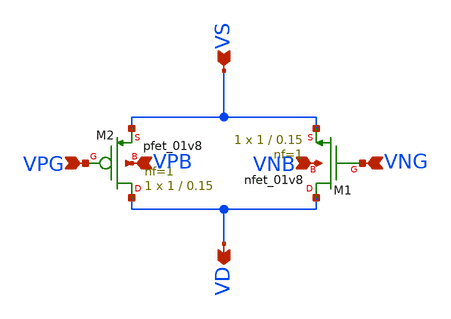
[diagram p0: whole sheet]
** sch_path: analog/schematics/Aswitch.sch
**.subckt Aswitch VPG VPB VNB VNG VS VD
*.ipin VPG
*.ipin VPB
*.ipin VNB
*.ipin VNG
*.ipin VS
*.opin VD
XM1 VD VNG VS VNB sky130_fd_pr__nfet_01v8 L=0.15 W=1 nf=1 ad='int((nf+1)/2) * W/nf * 0.29' as='int((nf+2)/2) * W/nf * 0.29'
+ pd='2*int((nf+1)/2) * (W/nf + 0.29)' ps='2*int((nf+2)/2) * (W/nf + 0.29)' nrd='0.29 / W' nrs='0.29 / W'
+ sa=0 sb=0 sd=0 mult=1 m=1
XM2 VD VPG VS VPB sky130_fd_pr__pfet_01v8 L=0.15 W=1 nf=1 ad='int((nf+1)/2) * W/nf * 0.29' as='int((nf+2)/2) * W/nf * 0.29'
+ pd='2*int((nf+1)/2) * (W/nf + 0.29)' ps='2*int((nf+2)/2) * (W/nf + 0.29)' nrd='0.29 / W' nrs='0.29 / W'
+ sa=0 sb=0 sd=0 mult=1 m=1
**.ends
.end
